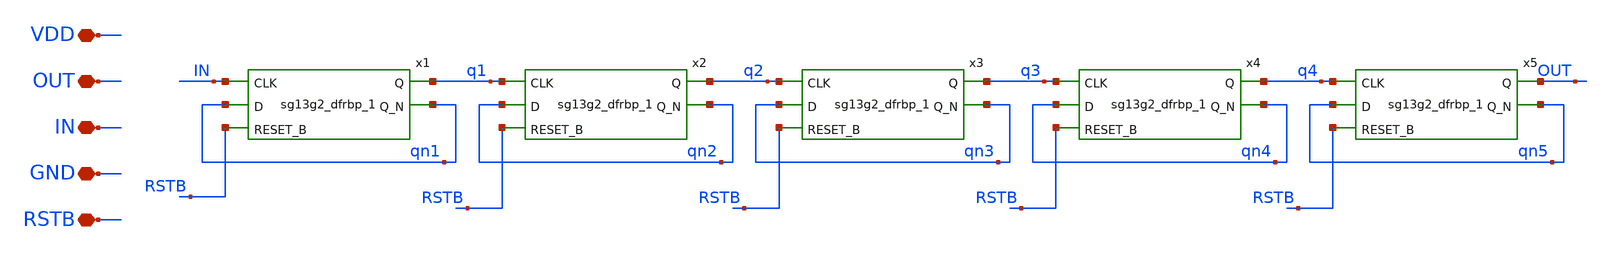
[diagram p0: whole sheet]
** sch_path: unic_cass_wrapper_user_project/ROs_reliability/div_sg13g2_stdcells.sch
**.subckt div_sg13g2_stdcells GND IN VDD OUT RSTB
*.iopin GND
*.iopin IN
*.iopin VDD
*.iopin OUT
*.iopin RSTB
x2 q2 qn2 q1 qn2 RSTB VDD GND sg13g2_dfrbp_1
x1 q1 qn1 IN qn1 RSTB VDD GND sg13g2_dfrbp_1
x3 q3 qn3 q2 qn3 RSTB VDD GND sg13g2_dfrbp_1
x4 q4 qn4 q3 qn4 RSTB VDD GND sg13g2_dfrbp_1
x5 OUT qn5 q4 qn5 RSTB VDD GND sg13g2_dfrbp_1
**.ends

* expanding   symbol:  sg13g2_stdcells/sg13g2_dfrbp_1.sym # of pins=5
** sym_path: sg13g2_stdcells/sg13g2_dfrbp_1.sym
** sch_path: sg13g2_stdcells/sg13g2_dfrbp_1.sch
.subckt sg13g2_dfrbp_1 Q Q_N CLK D RESET_B VDD VSS
*.ipin D
*.ipin RESET_B
*.ipin CLK
*.opin Q
*.opin Q_N
*.iopin VDD
*.iopin VSS
XM1 Db D net10 VSS sg13_lv_nmos w=420.00n l=130.00n ng=1 m=1 mm_ok=1
XM2 net10 RESET_B VSS VSS sg13_lv_nmos w=420.00n l=130.00n ng=1 m=1 mm_ok=1
XM3 net1 clkneg net9 VSS sg13_lv_nmos w=420.00n l=130.00n ng=1 m=1 mm_ok=1
XM4 net9 net1 VSS VSS sg13_lv_nmos w=420.00n l=130.00n ng=1 m=1 mm_ok=1
XM5 net1 net1 net5 VSS sg13_lv_nmos w=420.00n l=130.00n ng=1 m=1 mm_ok=1
XM6 net5 RESET_B VSS VSS sg13_lv_nmos w=420.00n l=130.00n ng=1 m=1 mm_ok=1
XM7 Q_N net1 VSS VSS sg13_lv_nmos w=740.00n l=130.00n ng=1 m=1 mm_ok=1
XM8 net2 net1 VSS VSS sg13_lv_nmos w=740.00n l=130.00n ng=1 m=1 mm_ok=1
XM9 Q net2 VSS VSS sg13_lv_nmos w=740.00n l=130.00n ng=1 m=1 mm_ok=1
XM10 clkneg CLK VSS VSS sg13_lv_nmos w=740.00n l=130.00n ng=1 m=1 mm_ok=1
XM11 clkpos clkneg VSS VSS sg13_lv_nmos w=740.00n l=130.00n ng=1 m=1 mm_ok=1
XM12 Db clkneg net3 VSS sg13_lv_nmos w=420.00n l=130.00n ng=1 m=1 mm_ok=1
XM13 net3 clkpos net8 VSS sg13_lv_nmos w=420.00n l=130.00n ng=1 m=1 mm_ok=1
XM14 net8 net3 net4 VSS sg13_lv_nmos w=420.00n l=130.00n ng=1 m=1 mm_ok=1
XM15 net4 RESET_B VSS VSS sg13_lv_nmos w=420.00n l=130.00n ng=1 m=1 mm_ok=1
XM16 net3 net3 VSS VSS sg13_lv_nmos w=740.00n l=130.00n ng=1 m=1 mm_ok=1
XM17 net3 clkpos net1 VSS sg13_lv_nmos w=740.00n l=130.00n ng=1 m=1 mm_ok=1
XM18 Db RESET_B VDD VDD sg13_lv_pmos w=420.00n l=130.00n ng=1 m=1 mm_ok=1
XM19 Db D VDD VDD sg13_lv_pmos w=420.00n l=130.00n ng=1 m=1 mm_ok=1
XM20 net7 net1 VDD VDD sg13_lv_pmos w=420.00n l=130.00n ng=1 m=1 mm_ok=1
XM21 net1 clkpos net7 VDD sg13_lv_pmos w=420.00n l=130.00n ng=1 m=1 mm_ok=1
XM22 net1 net1 VDD VDD sg13_lv_pmos w=420.00n l=130.00n ng=1 m=1 mm_ok=1
XM23 net1 RESET_B VDD VDD sg13_lv_pmos w=420.00n l=130.00n ng=1 m=1 mm_ok=1
XM24 Q_N net1 VDD VDD sg13_lv_pmos w=1.12u l=130.00n ng=1 m=1 mm_ok=1
XM25 net2 net1 VDD VDD sg13_lv_pmos w=1.12u l=130.00n ng=1 m=1 mm_ok=1
XM26 Q net2 VDD VDD sg13_lv_pmos w=1.12u l=130.00n ng=1 m=1 mm_ok=1
XM27 clkneg CLK VDD VDD sg13_lv_pmos w=1.12u l=130.00n ng=1 m=1 mm_ok=1
XM28 clkpos clkneg VDD VDD sg13_lv_pmos w=1.12u l=130.00n ng=1 m=1 mm_ok=1
XM29 Db clkpos net3 VDD sg13_lv_pmos w=420.00n l=130.00n ng=1 m=1 mm_ok=1
XM30 net6 net3 VDD VDD sg13_lv_pmos w=420.00n l=130.00n ng=1 m=1 mm_ok=1
XM31 net3 clkneg net6 VDD sg13_lv_pmos w=420.00n l=130.00n ng=1 m=1 mm_ok=1
XM32 net3 RESET_B VDD VDD sg13_lv_pmos w=420.00n l=130.00n ng=1 m=1 mm_ok=1
XM33 net3 net3 VDD VDD sg13_lv_pmos w=1.000u l=130.00n ng=1 m=1 mm_ok=1
XM34 net3 clkneg net1 VDD sg13_lv_pmos w=1.000u l=130.00n ng=1 m=1 mm_ok=1
.ends

.end
